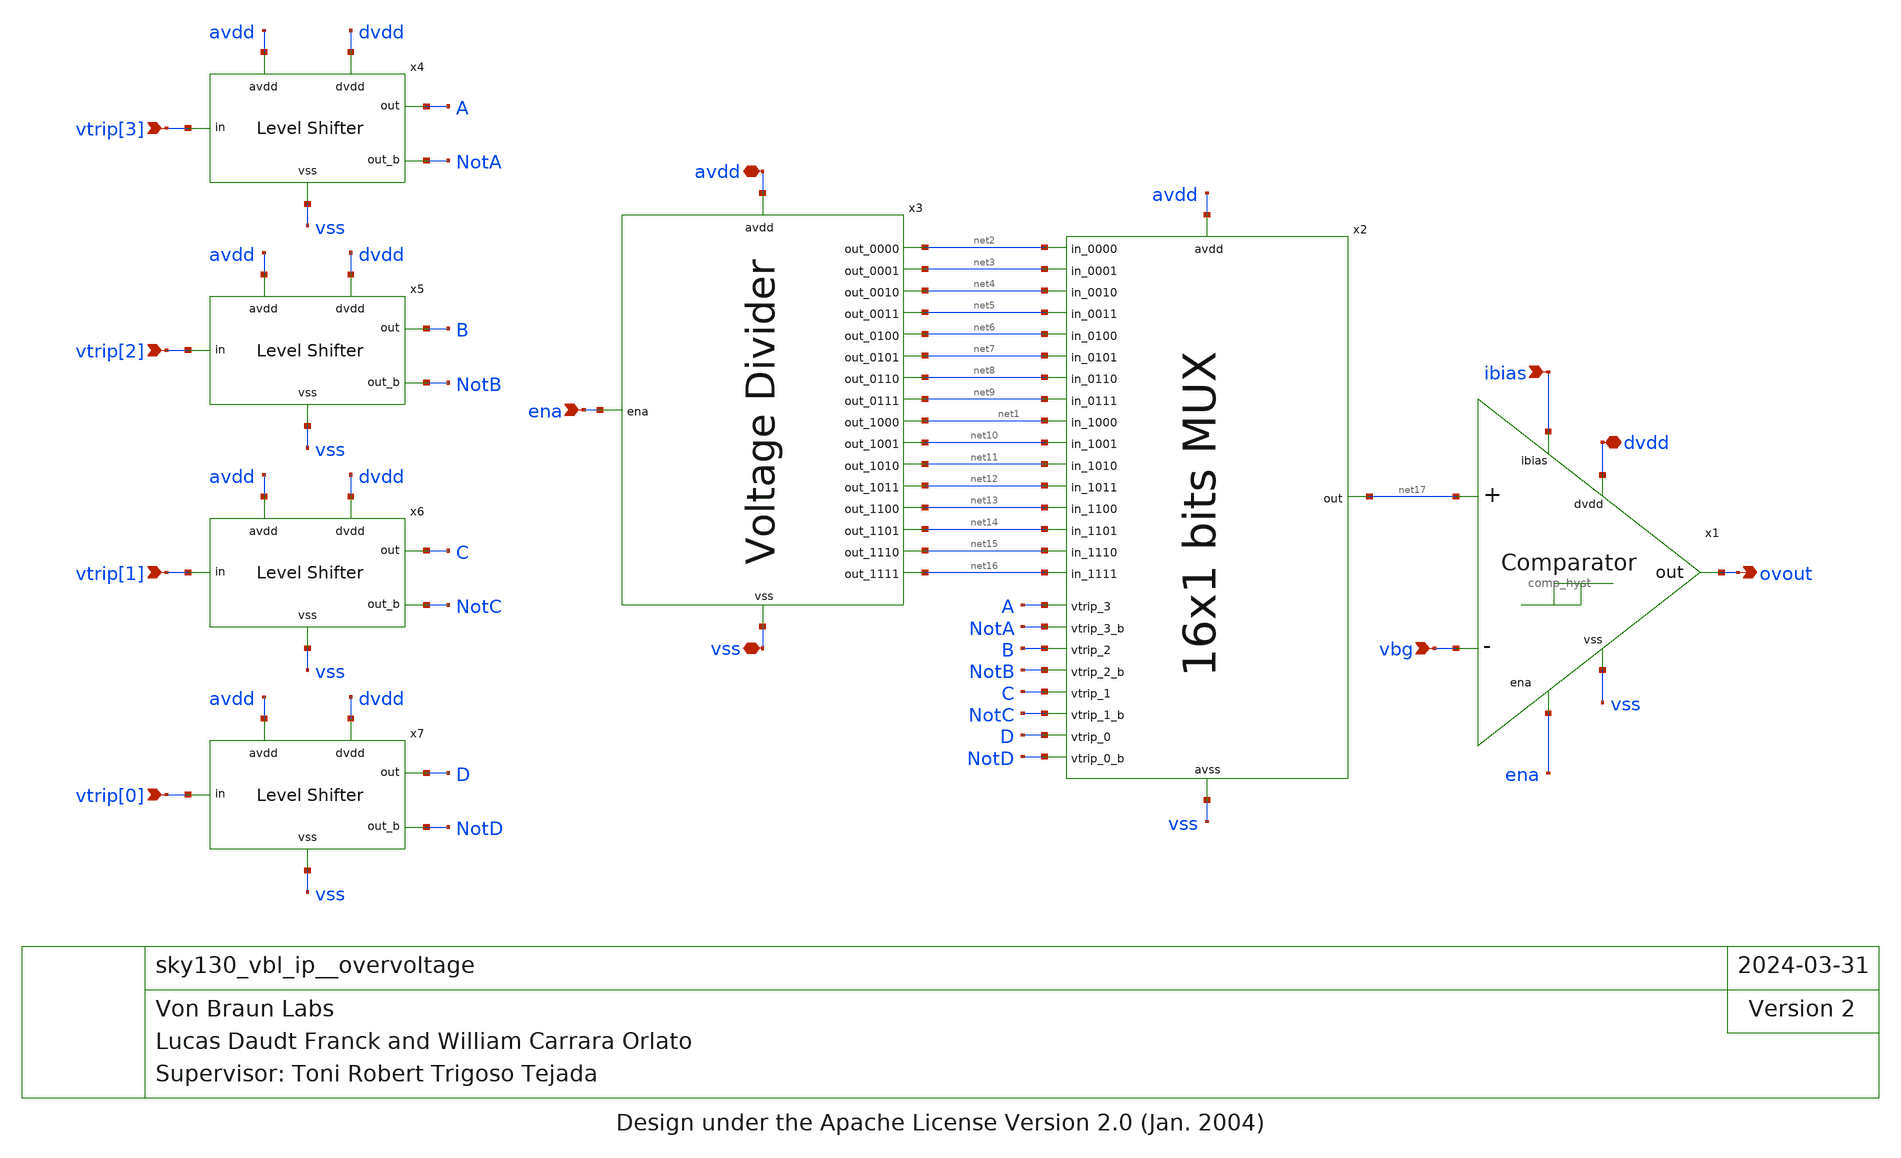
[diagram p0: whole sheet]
** sch_path: xschem/sky130_vbl_ip__overvoltage.sch
* Design under the Apache License Version 2.0 (Jan. 2004)
**.subckt sky130_vbl_ip__overvoltage avdd dvdd ena vss vtrip[3] ovout vbg vtrip[2] vtrip[1] vtrip[0]
*+ ibias
*.iopin avdd
*.iopin dvdd
*.ipin ena
*.iopin vss
*.ipin vtrip[3]
*.opin ovout
*.ipin vbg
*.ipin vtrip[2]
*.ipin vtrip[1]
*.ipin vtrip[0]
*.ipin ibias
x1 dvdd ovout vbg net17 ena ibias vss comp_hyst
x2 net2 net3 net4 net5 net6 net7 net8 avdd vss net9 A NotA B NotB C net17 NotC D NotD net1 net10
+ net11 net12 net13 net14 net15 net16 multiplexer
x3 avdd net2 net3 net4 net5 net6 net7 net8 net9 net1 net10 net11 net12 net13 net14 net15 net16 vss
+ ena voltage_divider
x4 avdd dvdd vtrip[3] A NotA vss level_shifter
x5 avdd dvdd vtrip[2] B NotB vss level_shifter
x6 avdd dvdd vtrip[1] C NotC vss level_shifter
x7 avdd dvdd vtrip[0] D NotD vss level_shifter
**.ends
.end
